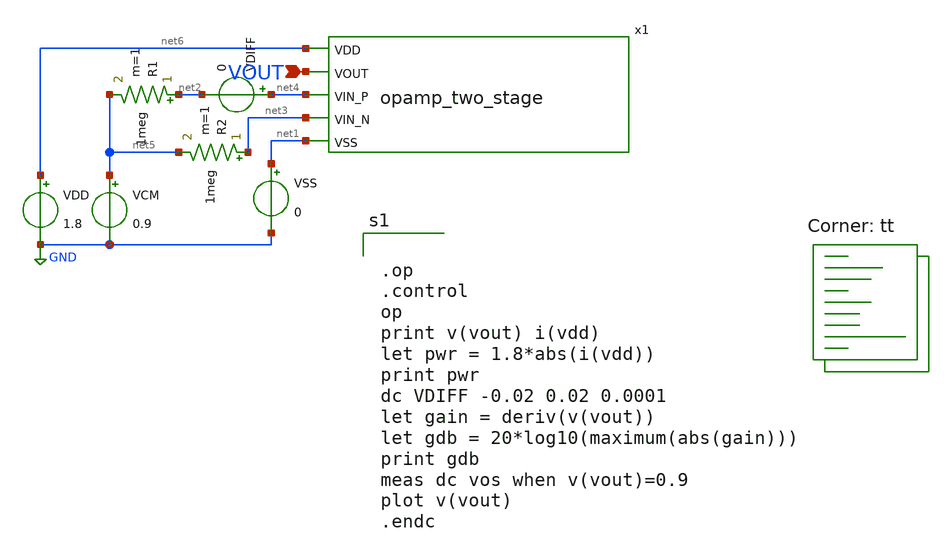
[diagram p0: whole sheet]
** sch_path: analog/bootcamp_opamp/schematics/opamp_two_stage_tb.sch
**.subckt opamp_two_stage_tb VOUT
*.ipin VOUT
VDD net6 GND 1.8
VSS net1 GND 0
VCM net5 GND 0.9
VDIFF net4 net2 0
R1 net2 net5 1meg m=1
R2 net3 net5 1meg m=1
x1 net6 VOUT net4 net3 net1 opamp_two_stage
**** begin user architecture code


.op
.control
op
print v(vout) i(vdd)
let pwr = 1.8*abs(i(vdd))
print pwr
dc VDIFF -0.02 0.02 0.0001
let gain = deriv(v(vout))
let gdb = 20*log10(maximum(abs(gain)))
print gdb
meas dc vos when v(vout)=0.9
plot v(vout)
.endc

.lib $::SKYWATER_MODELS/sky130.lib.spice tt
**** end user architecture code
**.ends

* expanding   symbol:  opamp_two_stage.sym # of pins=5
** sym_path: analog/bootcamp_opamp/schematics/opamp_two_stage.sym
** sch_path: analog/bootcamp_opamp/schematics/opamp_two_stage.sch
.subckt opamp_two_stage VDD VOUT VIN_P VIN_N VSS
*.ipin VIN_N
*.ipin VIN_P
*.ipin VDD
*.ipin VSS
*.ipin VOUT
XMN1 net2 VIN_N net1 VSS sky130_fd_pr__nfet_01v8 L=1 W=20 nf=1 ad='int((nf+1)/2) * W/nf * 0.29' as='int((nf+2)/2) * W/nf * 0.29'
+ pd='2*int((nf+1)/2) * (W/nf + 0.29)' ps='2*int((nf+2)/2) * (W/nf + 0.29)' nrd='0.29 / W' nrs='0.29 / W'
+ sa=0 sb=0 sd=0 mult=1 m=1
XMP1 net2 net2 VDD VDD sky130_fd_pr__pfet_01v8 L=1 W=10 nf=1 ad='int((nf+1)/2) * W/nf * 0.29' as='int((nf+2)/2) * W/nf * 0.29'
+ pd='2*int((nf+1)/2) * (W/nf + 0.29)' ps='2*int((nf+2)/2) * (W/nf + 0.29)' nrd='0.29 / W' nrs='0.29 / W'
+ sa=0 sb=0 sd=0 mult=1 m=1
XMP2 net3 net2 VDD VDD sky130_fd_pr__pfet_01v8 L=1 W=10 nf=1 ad='int((nf+1)/2) * W/nf * 0.29' as='int((nf+2)/2) * W/nf * 0.29'
+ pd='2*int((nf+1)/2) * (W/nf + 0.29)' ps='2*int((nf+2)/2) * (W/nf + 0.29)' nrd='0.29 / W' nrs='0.29 / W'
+ sa=0 sb=0 sd=0 mult=1 m=1
XMN2 net3 VIN_P net1 VSS sky130_fd_pr__nfet_01v8 L=1 W=20 nf=1 ad='int((nf+1)/2) * W/nf * 0.29' as='int((nf+2)/2) * W/nf * 0.29'
+ pd='2*int((nf+1)/2) * (W/nf + 0.29)' ps='2*int((nf+2)/2) * (W/nf + 0.29)' nrd='0.29 / W' nrs='0.29 / W'
+ sa=0 sb=0 sd=0 mult=1 m=1
XMNB net1 net5 VSS VSS sky130_fd_pr__nfet_01v8 L=1 W=4 nf=1 ad='int((nf+1)/2) * W/nf * 0.29' as='int((nf+2)/2) * W/nf * 0.29'
+ pd='2*int((nf+1)/2) * (W/nf + 0.29)' ps='2*int((nf+2)/2) * (W/nf + 0.29)' nrd='0.29 / W' nrs='0.29 / W'
+ sa=0 sb=0 sd=0 mult=2 m=2
XMPO VOUT net3 VDD VDD sky130_fd_pr__pfet_01v8 L=0.15 W=15 nf=1 ad='int((nf+1)/2) * W/nf * 0.29' as='int((nf+2)/2) * W/nf * 0.29'
+ pd='2*int((nf+1)/2) * (W/nf + 0.29)' ps='2*int((nf+2)/2) * (W/nf + 0.29)' nrd='0.29 / W' nrs='0.29 / W'
+ sa=0 sb=0 sd=0 mult=8 m=8
XR1 net4 net3 sky130_fd_pr__res_generic_po W=1 L=2.5 m=1
XC1 net4 VOUT sky130_fd_pr__cap_mim_m3_1 W=22 L=22 MF=1 m=1
XMB VOUT net5 VSS VSS sky130_fd_pr__nfet_01v8 L=0.15 W=6 nf=1 ad='int((nf+1)/2) * W/nf * 0.29' as='int((nf+2)/2) * W/nf * 0.29'
+ pd='2*int((nf+1)/2) * (W/nf + 0.29)' ps='2*int((nf+2)/2) * (W/nf + 0.29)' nrd='0.29 / W' nrs='0.29 / W'
+ sa=0 sb=0 sd=0 mult=8 m=8
XR2 net5 VDD VSS sky130_fd_pr__res_xhigh_po_0p69 L=16 mult=1 m=1
XMB1 net5 net5 VSS VSS sky130_fd_pr__nfet_01v8 L=1 W=4 nf=1 ad='int((nf+1)/2) * W/nf * 0.29' as='int((nf+2)/2) * W/nf * 0.29'
+ pd='2*int((nf+1)/2) * (W/nf + 0.29)' ps='2*int((nf+2)/2) * (W/nf + 0.29)' nrd='0.29 / W' nrs='0.29 / W'
+ sa=0 sb=0 sd=0 mult=1 m=1
.ends

.GLOBAL GND
.end
